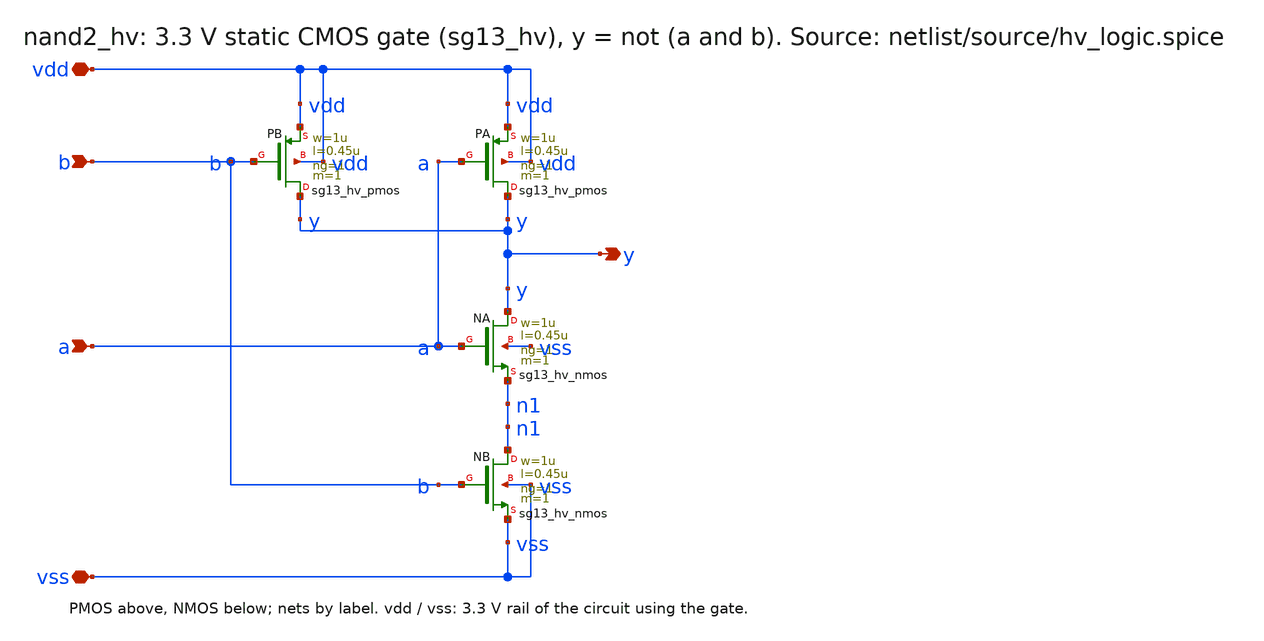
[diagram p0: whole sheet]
** sch_path: macros/hv_logic/schematic/xschem/nand2_hv.sch
**.subckt nand2_hv vdd vss a b y
*.iopin vdd
*.iopin vss
*.ipin a
*.ipin b
*.opin y
XPA y a vdd vdd sg13_hv_pmos w=1u l=0.45u ng=1 m=1 mm_ok=1
XPB y b vdd vdd sg13_hv_pmos w=1u l=0.45u ng=1 m=1 mm_ok=1
XNA y a n1 vss sg13_hv_nmos w=1u l=0.45u ng=1 m=1 mm_ok=1
XNB n1 b vss vss sg13_hv_nmos w=1u l=0.45u ng=1 m=1 mm_ok=1
**.ends
.end
